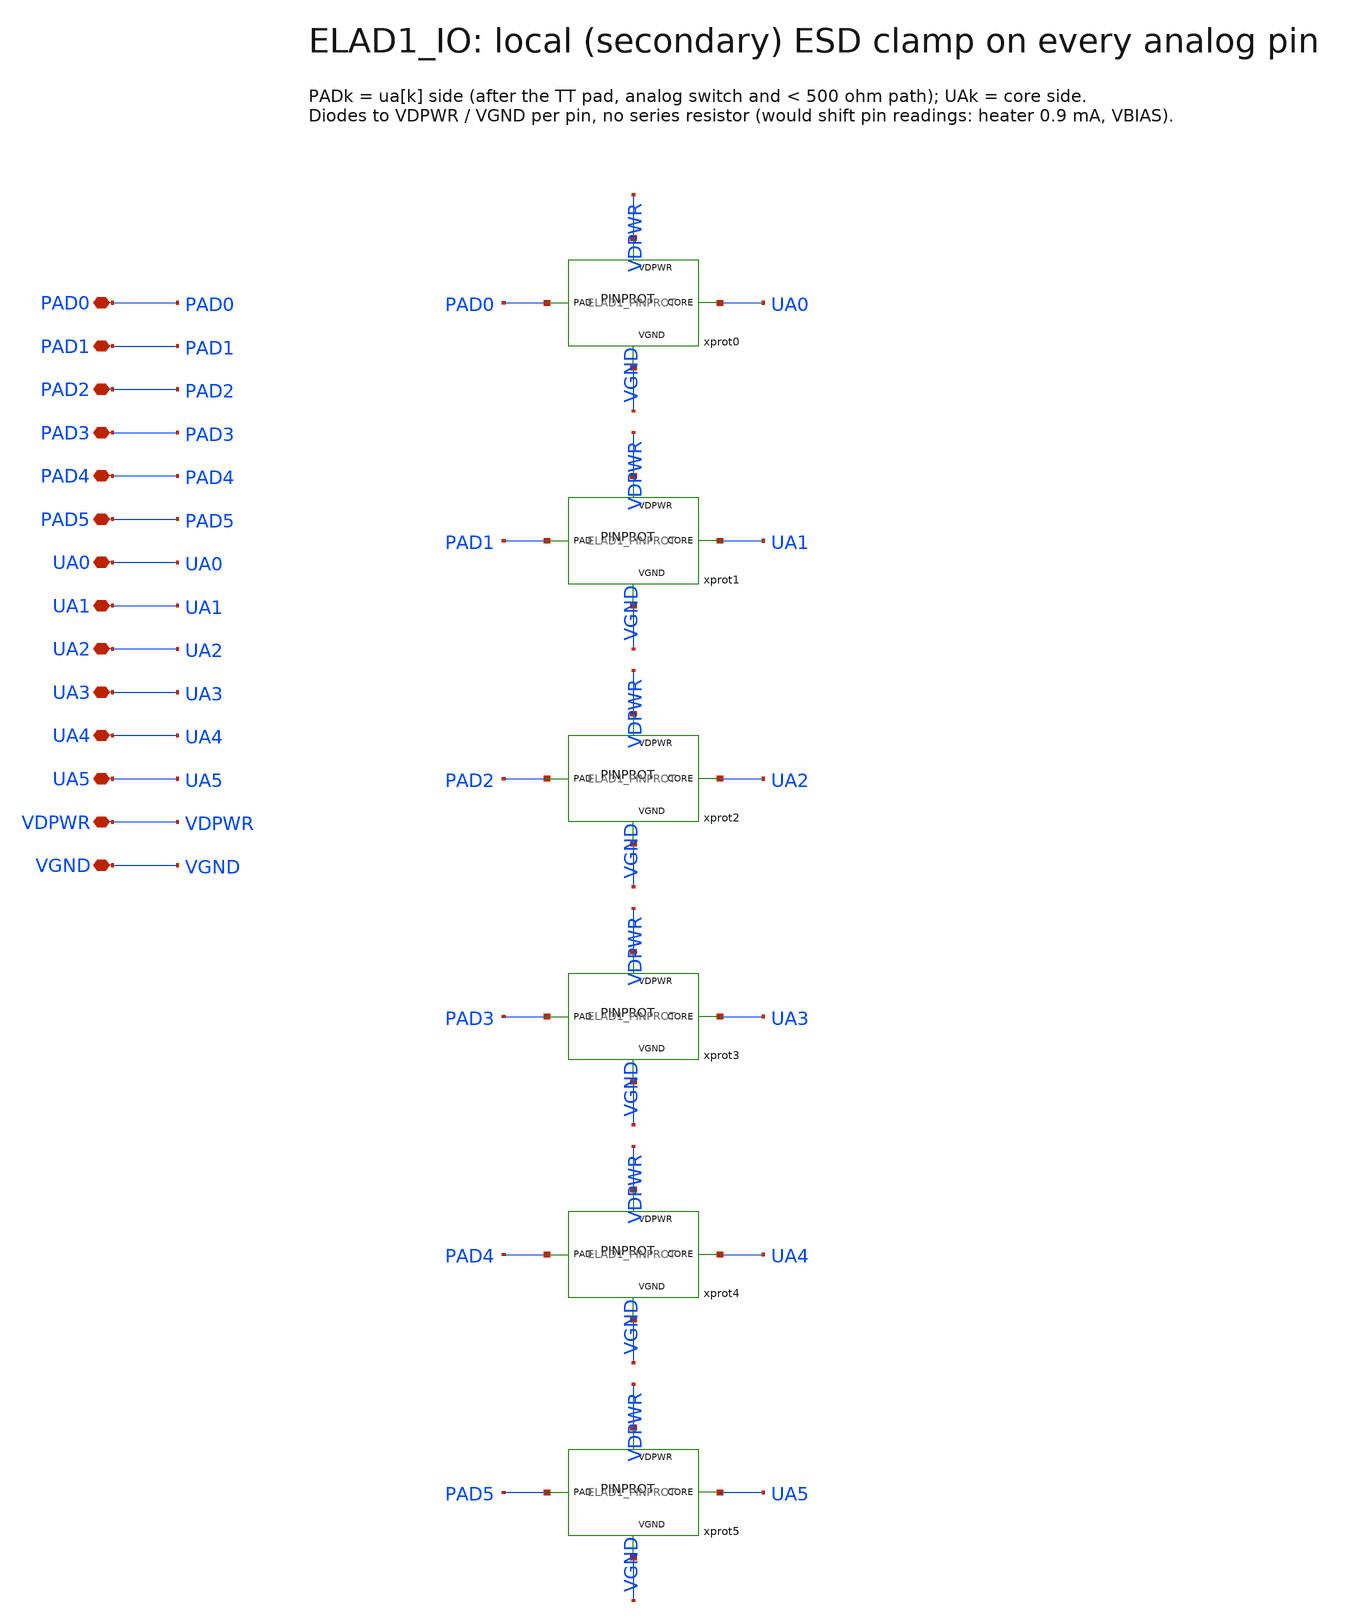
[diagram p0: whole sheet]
** sch_path: cells/ELAD1_IO/schematic/ELAD1_IO.sch
**.subckt ELAD1_IO PAD0 PAD1 PAD2 PAD3 PAD4 PAD5 UA0 UA1 UA2 UA3 UA4 UA5 VDPWR VGND
*.iopin PAD0
*.iopin PAD1
*.iopin PAD2
*.iopin PAD3
*.iopin PAD4
*.iopin PAD5
*.iopin UA0
*.iopin UA1
*.iopin UA2
*.iopin UA3
*.iopin UA4
*.iopin UA5
*.iopin VDPWR
*.iopin VGND
xprot0 PAD0 UA0 VDPWR VGND ELAD1_PINPROT
xprot1 PAD1 UA1 VDPWR VGND ELAD1_PINPROT
xprot2 PAD2 UA2 VDPWR VGND ELAD1_PINPROT
xprot3 PAD3 UA3 VDPWR VGND ELAD1_PINPROT
xprot4 PAD4 UA4 VDPWR VGND ELAD1_PINPROT
xprot5 PAD5 UA5 VDPWR VGND ELAD1_PINPROT
**.ends

* expanding   symbol:  ELAD1_PINPROT.sym # of pins=4
** sym_path: cells/ELAD1_PINPROT/schematic/ELAD1_PINPROT.sym
** sch_path: cells/ELAD1_PINPROT/schematic/ELAD1_PINPROT.sch
.subckt ELAD1_PINPROT PAD CORE VDPWR VGND
*.iopin PAD
*.iopin CORE
*.iopin VDPWR
*.iopin VGND
RLINK PAD CORE 0.001 m=1
XDP PAD VDPWR sky130_fd_pr__diode_pd2nw_05v5 area=36 pj=4e6
XDN VGND PAD sky130_fd_pr__diode_pw2nd_05v5 area=36 pj=4e6
.ends

.end
